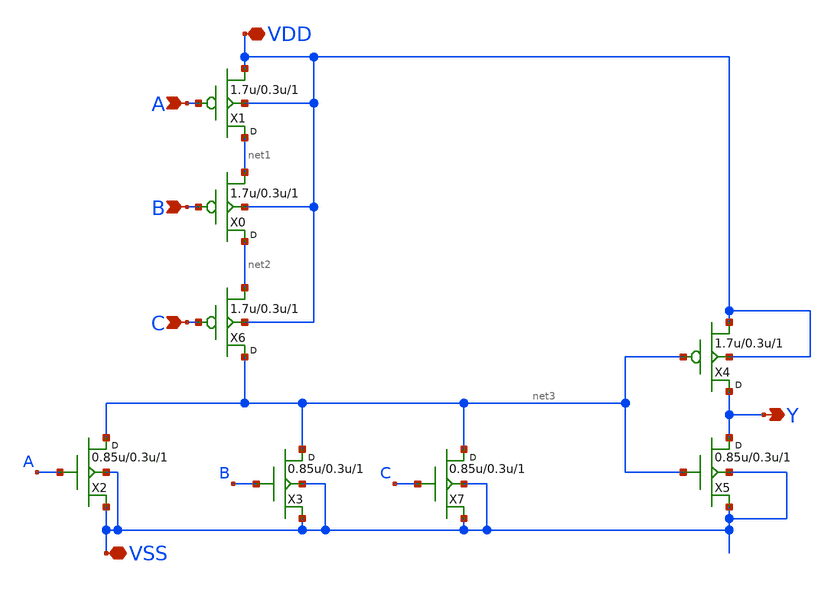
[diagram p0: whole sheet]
** sch_path: new/12t_or3_1.sch
**.subckt 12t_or3_1 A B C Y VDD VSS
*.ipin A
*.ipin B
*.ipin C
*.opin Y
*.iopin VDD
*.iopin VSS
X1 net1 A VDD VDD pfet_03p3 w=1.7u l=0.3u m=1
X0 net2 B net1 VDD pfet_03p3 w=1.7u l=0.3u m=1
X6 net3 C net2 VDD pfet_03p3 w=1.7u l=0.3u m=1
X2 net3 A VSS VSS nfet_03p3 w=0.85u l=0.3u m=1
X3 net3 B VSS VSS nfet_03p3 w=0.85u l=0.3u m=1
X7 net3 C VSS VSS nfet_03p3 w=0.85u l=0.3u m=1
X4 Y net3 VDD VDD pfet_03p3 w=1.7u l=0.3u m=1
X5 Y net3 VSS VSS nfet_03p3 w=0.85u l=0.3u m=1
**.ends
.end
